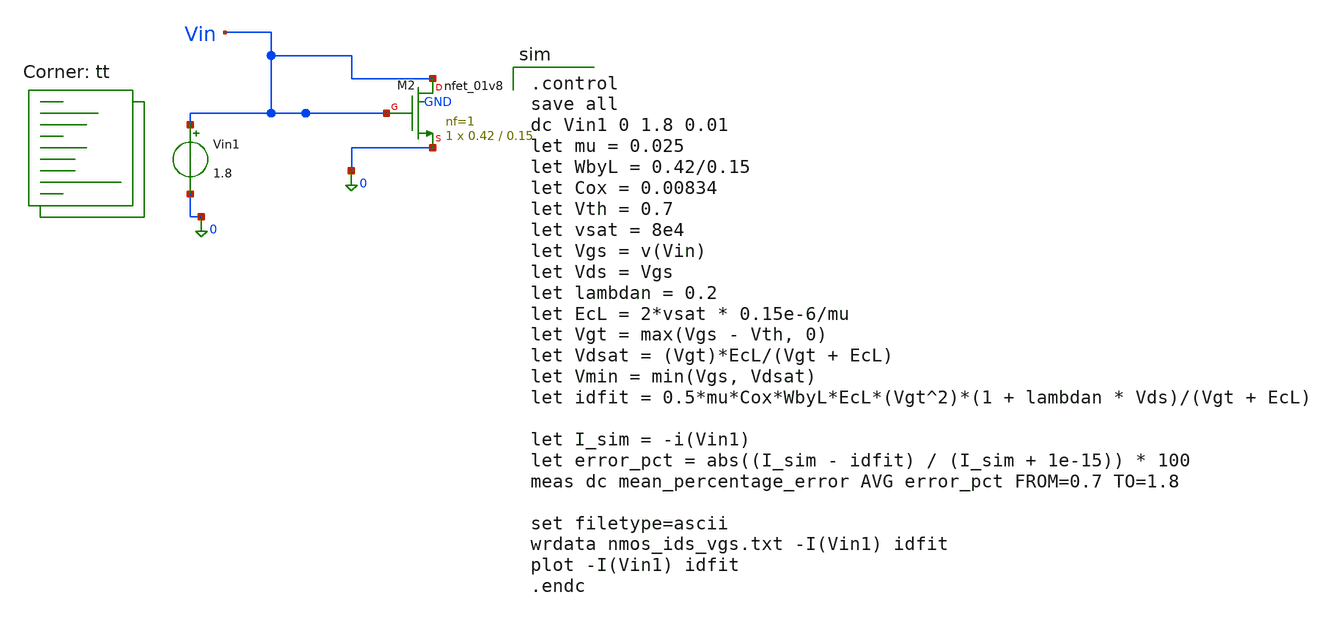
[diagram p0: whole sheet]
** sch_path: tutorial-1/source/q1.sch
**.subckt q1
Vin1 Vin 0 1.8
XM2 Vin Vin 0 GND sky130_fd_pr__nfet_01v8 L=0.15 W=0.42 nf=1 ad='int((nf+1)/2) * W/nf * 0.29' as='int((nf+2)/2) * W/nf * 0.29'
+ pd='2*int((nf+1)/2) * (W/nf + 0.29)' ps='2*int((nf+2)/2) * (W/nf + 0.29)' nrd='0.29 / W' nrs='0.29 / W'
+ sa=0 sb=0 sd=0 mult=1 m=1
**** begin user architecture code
.lib $::SKYWATER_MODELS/sky130.lib.spice tt

.control
save all
dc Vin1 0 1.8 0.01
let mu = 0.025
let WbyL = 0.42/0.15
let Cox = 0.00834
let Vth = 0.7
let vsat = 8e4
let Vgs = v(Vin)
let Vds = Vgs
let lambdan = 0.2
let EcL = 2*vsat * 0.15e-6/mu
let Vgt = max(Vgs - Vth, 0)
let Vdsat = (Vgt)*EcL/(Vgt + EcL)
let Vmin = min(Vgs, Vdsat)
let idfit = 0.5*mu*Cox*WbyL*EcL*(Vgt^2)*(1 + lambdan * Vds)/(Vgt + EcL)

let I_sim = -i(Vin1)
let error_pct = abs((I_sim - idfit) / (I_sim + 1e-15)) * 100
meas dc mean_percentage_error AVG error_pct FROM=0.7 TO=1.8

set filetype=ascii
wrdata nmos_ids_vgs.txt -I(Vin1) idfit
plot -I(Vin1) idfit
.endc

**** end user architecture code
**.ends
.end
